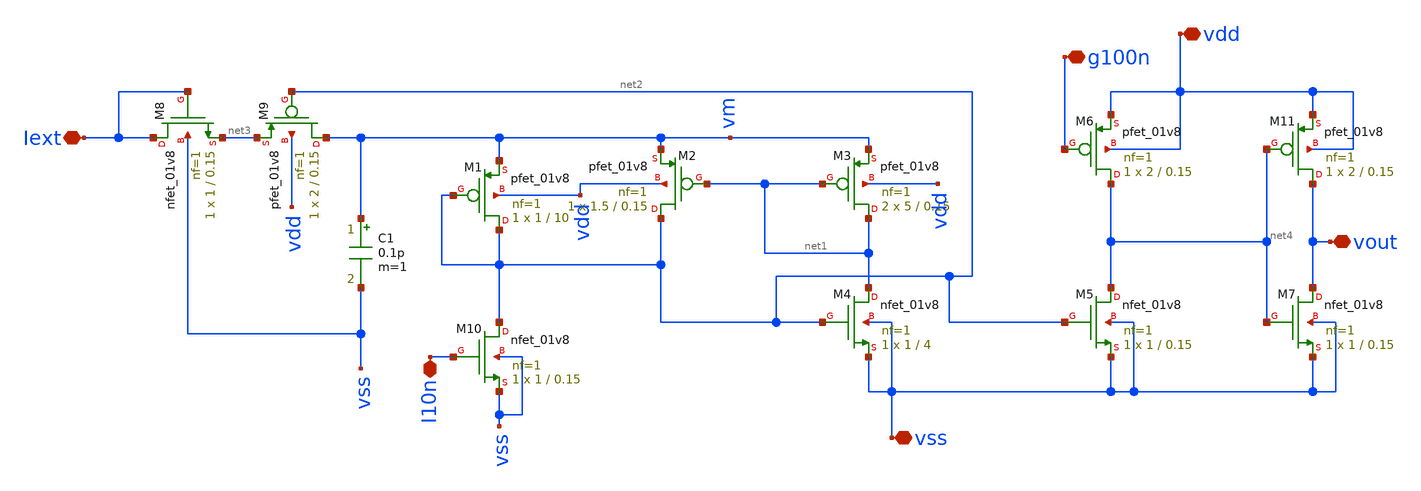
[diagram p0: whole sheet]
** sch_path: Neuron/ultralif/ultralif.sch
**.subckt ultralif Iext vout vss I10n vdd g100n
*.iopin Iext
*.iopin vout
*.iopin vss
*.iopin I10n
*.iopin vdd
*.iopin g100n
XM1 net2 net2 vm vdd sky130_fd_pr__pfet_01v8 L=10 W=1 nf=1 ad='int((nf+1)/2) * W/nf * 0.29' as='int((nf+2)/2) * W/nf * 0.29'
+ pd='2*int((nf+1)/2) * (W/nf + 0.29)' ps='2*int((nf+2)/2) * (W/nf + 0.29)' nrd='0.29 / W' nrs='0.29 / W'
+ sa=0 sb=0 sd=0 mult=1 m=1
XM2 net2 net1 vm vdd sky130_fd_pr__pfet_01v8 L=0.15 W=1.5 nf=1 ad='int((nf+1)/2) * W/nf * 0.29' as='int((nf+2)/2) * W/nf * 0.29'
+ pd='2*int((nf+1)/2) * (W/nf + 0.29)' ps='2*int((nf+2)/2) * (W/nf + 0.29)' nrd='0.29 / W' nrs='0.29 / W'
+ sa=0 sb=0 sd=0 mult=1 m=1
XM3 net1 net1 vm vdd sky130_fd_pr__pfet_01v8 L=0.15 W=5 nf=1 ad='int((nf+1)/2) * W/nf * 0.29' as='int((nf+2)/2) * W/nf * 0.29'
+ pd='2*int((nf+1)/2) * (W/nf + 0.29)' ps='2*int((nf+2)/2) * (W/nf + 0.29)' nrd='0.29 / W' nrs='0.29 / W'
+ sa=0 sb=0 sd=0 mult=2 m=2
XM4 net1 net2 vss vss sky130_fd_pr__nfet_01v8 L=4 W=1 nf=1 ad='int((1 + 1)/2) * 1 / 1 * 0.29' as='int((1 + 2)/2) * 1 / 1 * 0.29'
+ pd='2*int((1 + 1)/2) * (1 / 1 + 0.29)' ps='2*int((1 + 2)/2) * (1 / 1 + 0.29)' nrd='0.29 / 1 ' nrs='0.29 / 1 '
+ sa=0 sb=0 sd=0 mult=1 m=1
C1 vm vss 0.1p m=1
XM9 vm net2 net3 vdd sky130_fd_pr__pfet_01v8 L=0.15 W=2 nf=1 ad='int((nf+1)/2) * W/nf * 0.29' as='int((nf+2)/2) * W/nf * 0.29'
+ pd='2*int((nf+1)/2) * (W/nf + 0.29)' ps='2*int((nf+2)/2) * (W/nf + 0.29)' nrd='0.29 / W' nrs='0.29 / W'
+ sa=0 sb=0 sd=0 mult=1 m=1
XM10 net2 I10n vss vss sky130_fd_pr__nfet_01v8 L=0.15 W=1 nf=1 ad='int((1 + 1)/2) * 1 / 1 * 0.29' as='int((1 + 2)/2) * 1 / 1 * 0.29'
+ pd='2*int((1 + 1)/2) * (1 / 1 + 0.29)' ps='2*int((1 + 2)/2) * (1 / 1 + 0.29)' nrd='0.29 / 1 ' nrs='0.29 / 1 '
+ sa=0 sb=0 sd=0 mult=1 m=1
XM5 net4 net2 vss vss sky130_fd_pr__nfet_01v8 L=0.15 W=1 nf=1 ad='int((1 + 1)/2) * 1 / 1 * 0.29' as='int((1 + 2)/2) * 1 / 1 * 0.29'
+ pd='2*int((1 + 1)/2) * (1 / 1 + 0.29)' ps='2*int((1 + 2)/2) * (1 / 1 + 0.29)' nrd='0.29 / 1 ' nrs='0.29 / 1 '
+ sa=0 sb=0 sd=0 mult=1 m=1
XM6 net4 g100n vdd vdd sky130_fd_pr__pfet_01v8 L=0.15 W=2 nf=1 ad='int((nf+1)/2) * W/nf * 0.29' as='int((nf+2)/2) * W/nf * 0.29'
+ pd='2*int((nf+1)/2) * (W/nf + 0.29)' ps='2*int((nf+2)/2) * (W/nf + 0.29)' nrd='0.29 / W' nrs='0.29 / W'
+ sa=0 sb=0 sd=0 mult=1 m=1
XM7 vout net4 vss vss sky130_fd_pr__nfet_01v8 L=0.15 W=1 nf=1 ad='int((1 + 1)/2) * 1 / 1 * 0.29' as='int((1 + 2)/2) * 1 / 1 * 0.29'
+ pd='2*int((1 + 1)/2) * (1 / 1 + 0.29)' ps='2*int((1 + 2)/2) * (1 / 1 + 0.29)' nrd='0.29 / 1 ' nrs='0.29 / 1 '
+ sa=0 sb=0 sd=0 mult=1 m=1
XM11 vout net4 vdd vdd sky130_fd_pr__pfet_01v8 L=0.15 W=2 nf=1 ad='int((nf+1)/2) * W/nf * 0.29' as='int((nf+2)/2) * W/nf * 0.29'
+ pd='2*int((nf+1)/2) * (W/nf + 0.29)' ps='2*int((nf+2)/2) * (W/nf + 0.29)' nrd='0.29 / W' nrs='0.29 / W'
+ sa=0 sb=0 sd=0 mult=1 m=1
XM8 Iext Iext net3 vss sky130_fd_pr__nfet_01v8 L=0.15 W=1 nf=1 ad='int((1 + 1)/2) * 1 / 1 * 0.29' as='int((1 + 2)/2) * 1 / 1 * 0.29'
+ pd='2*int((1 + 1)/2) * (1 / 1 + 0.29)' ps='2*int((1 + 2)/2) * (1 / 1 + 0.29)' nrd='0.29 / 1 ' nrs='0.29 / 1 '
+ sa=0 sb=0 sd=0 mult=1 m=1
**.ends
.end
